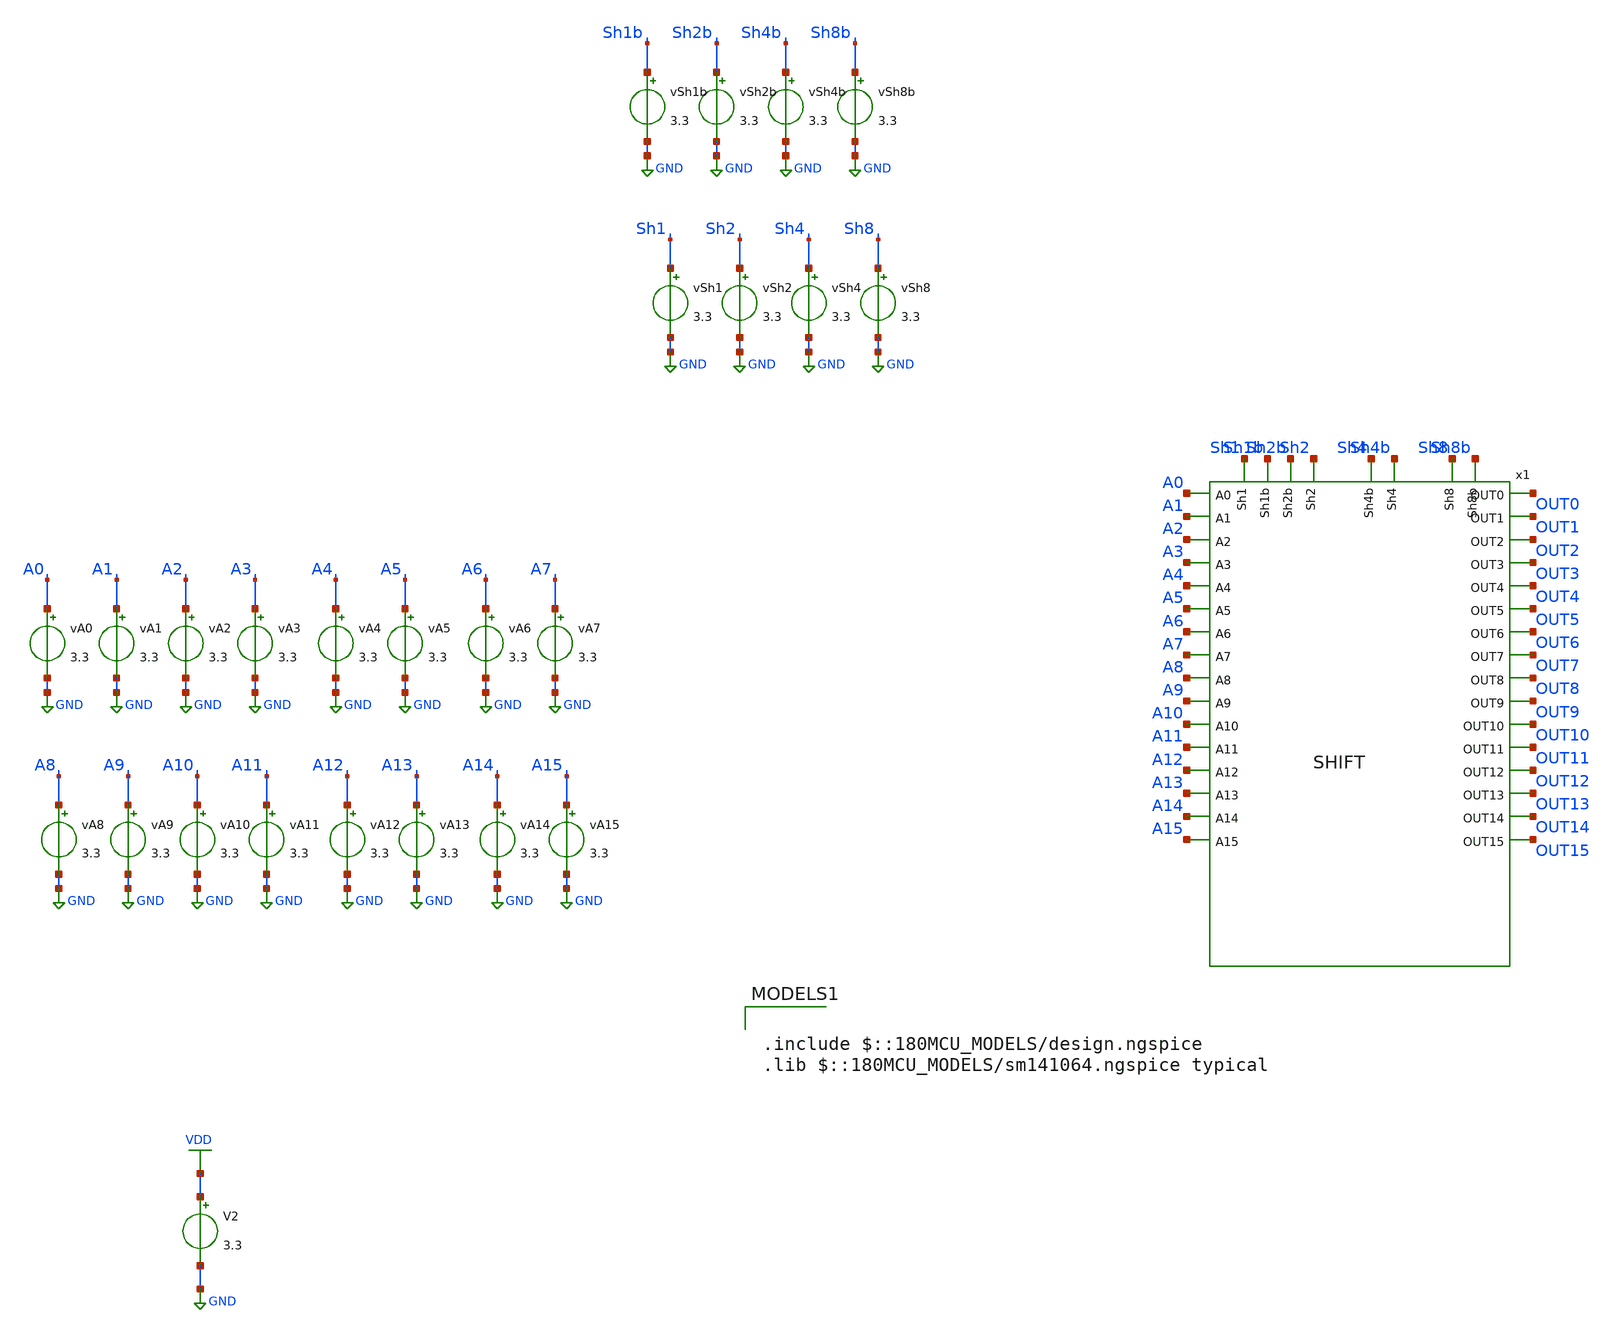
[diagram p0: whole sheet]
** sch_path: tbs/full_shift_tb.sch
**.subckt full_shift_tb
vA0 A0 GND 3.3
vA1 A1 GND 3.3
vA2 A2 GND 3.3
vA3 A3 GND 3.3
vA4 A4 GND 3.3
vA5 A5 GND 3.3
vA6 A6 GND 3.3
vA7 A7 GND 3.3
vA8 A8 GND 3.3
vA9 A9 GND 3.3
vA10 A10 GND 3.3
vA11 A11 GND 3.3
vA12 A12 GND 3.3
vA13 A13 GND 3.3
vA14 A14 GND 3.3
vA15 A15 GND 3.3
vSh1 Sh1 GND 3.3
vSh2 Sh2 GND 3.3
vSh4 Sh4 GND 3.3
vSh8 Sh8 GND 3.3
vSh1b Sh1b GND 3.3
vSh2b Sh2b GND 3.3
vSh4b Sh4b GND 3.3
vSh8b Sh8b GND 3.3
x1 Sh1b Sh1 Sh2 Sh2b A0 OUT0 A1 OUT1 Sh4b Sh4 A2 OUT2 A3 OUT3 Sh8b Sh8 OUT4 A4 OUT5 A5 OUT6 A6 OUT7
+ A7 OUT8 A8 A9 OUT9 A10 OUT10 OUT11 A11 OUT12 A12 A13 OUT13 OUT14 A14 OUT15 A15 SHIFT
V2 VDD GND 3.3
**** begin user architecture code

.include $::180MCU_MODELS/design.ngspice
.lib $::180MCU_MODELS/sm141064.ngspice typical



.control
let vlow = 0
let vhigh = 3.3

* A = 1010101010101010 = 43690
alter VA15 = $&vhigh
alter VA14 = $&vlow
alter VA13 = $&vhigh
alter VA12 = $&vlow
alter VA11 = $&vhigh
alter VA10 = $&vlow
alter VA9  = $&vhigh
alter VA8  = $&vlow
alter VA7  = $&vhigh
alter VA6  = $&vlow
alter VA5  = $&vhigh
alter VA4  = $&vlow
alter VA3  = $&vhigh
alter VA2  = $&vlow
alter VA1  = $&vhigh
alter VA0  = $&vlow

* --- Define Shift Control Values ---
alter vSh8 = $&vlow
alter vSh4 = $&vlow
alter vSh2 = $&vlow
alter vSh1 = $&vhigh
alter vSh8b = $&vhigh
alter vSh4b = $&vhigh
alter vSh2b = $&vhigh
alter vSh1b = $&vlow

* Run transient
tran 100n 100u

* --- Digitizing Input A (Measurement at 30ns) ---
meas tran a0  find v(A0)  at=30n
meas tran a1  find v(A1)  at=30n
meas tran a2  find v(A2)  at=30n
meas tran a3  find v(A3)  at=30n
meas tran a4  find v(A4)  at=30n
meas tran a5  find v(A5)  at=30n
meas tran a6  find v(A6)  at=30n
meas tran a7  find v(A7)  at=30n
meas tran a8  find v(A8)  at=30n
meas tran a9  find v(A9)  at=30n
meas tran a10 find v(A10) at=30n
meas tran a11 find v(A11) at=30n
meas tran a12 find v(A12) at=30n
meas tran a13 find v(A13) at=30n
meas tran a14 find v(A14) at=30n
meas tran a15 find v(A15) at=30n

* --- Digitizing Output (Measurement at 30ns) ---
meas tran v0  find v(OUT0)  at=30n
meas tran v1  find v(OUT1)  at=30n
meas tran v2  find v(OUT2)  at=30n
meas tran v3  find v(OUT3)  at=30n
meas tran v4  find v(OUT4)  at=30n
meas tran v5  find v(OUT5)  at=30n
meas tran v6  find v(OUT6)  at=30n
meas tran v7  find v(OUT7)  at=30n
meas tran v8  find v(OUT8)  at=30n
meas tran v9  find v(OUT9)  at=30n
meas tran v10 find v(OUT10) at=30n
meas tran v11 find v(OUT11) at=30n
meas tran v12 find v(OUT12) at=30n
meas tran v13 find v(OUT13) at=30n
meas tran v14 find v(OUT14) at=30n
meas tran v15 find v(OUT15) at=30n

* Initialize tracking variables
let input_A_decimal = 0
let decimal_result = 0

* Logic checks for Input A and Output
if a0 > 1.6 | let input_A_decimal = input_A_decimal + 1 | end
if v0 > 1.6 | let decimal_result = decimal_result + 1 | end

if a1 > 1.6 | let input_A_decimal = input_A_decimal + 2 | end
if v1 > 1.6 | let decimal_result = decimal_result + 2 | end

if a2 > 1.6 | let input_A_decimal = input_A_decimal + 4 | end
if v2 > 1.6 | let decimal_result = decimal_result + 4 | end

if a3 > 1.6 | let input_A_decimal = input_A_decimal + 8 | end
if v3 > 1.6 | let decimal_result = decimal_result + 8 | end

if a4 > 1.6 | let input_A_decimal = input_A_decimal + 16 | end
if v4 > 1.6 | let decimal_result = decimal_result + 16 | end

if a5 > 1.6 | let input_A_decimal = input_A_decimal + 32 | end
if v5 > 1.6 | let decimal_result = decimal_result + 32 | end

if a6 > 1.6 | let input_A_decimal = input_A_decimal + 64 | end
if v6 > 1.6 | let decimal_result = decimal_result + 64 | end

if a7 > 1.6 | let input_A_decimal = input_A_decimal + 128 | end
if v7 > 1.6 | let decimal_result = decimal_result + 128 | end

if a8 > 1.6 | let input_A_decimal = input_A_decimal + 256 | end
if v8 > 1.6 | let decimal_result = decimal_result + 256 | end

if a9 > 1.6 | let input_A_decimal = input_A_decimal + 512 | end
if v9 > 1.6 | let decimal_result = decimal_result + 512 | end

if a10 > 1.6 | let input_A_decimal = input_A_decimal + 1024 | end
if v10 > 1.6 | let decimal_result = decimal_result + 1024 | end

if a11 > 1.6 | let input_A_decimal = input_A_decimal + 2048 | end
if v11 > 1.6 | let decimal_result = decimal_result + 2048 | end

if a12 > 1.6 | let input_A_decimal = input_A_decimal + 4096 | end
if v12 > 1.6 | let decimal_result = decimal_result + 4096 | end

if a13 > 1.6 | let input_A_decimal = input_A_decimal + 8192 | end
if v13 > 1.6 | let decimal_result = decimal_result + 8192 | end

if a14 > 1.6 | let input_A_decimal = input_A_decimal + 16384 | end
if v14 > 1.6 | let decimal_result = decimal_result + 16384 | end

if a15 > 1.6 | let input_A_decimal = input_A_decimal + 32768 | end
if v15 > 1.6 | let decimal_result = decimal_result + 32768 | end

* --- Output Results ---
print input_A_decimal
print decimal_result
.endc


**** end user architecture code
**.ends
.GLOBAL GND
.GLOBAL VDD
.end
